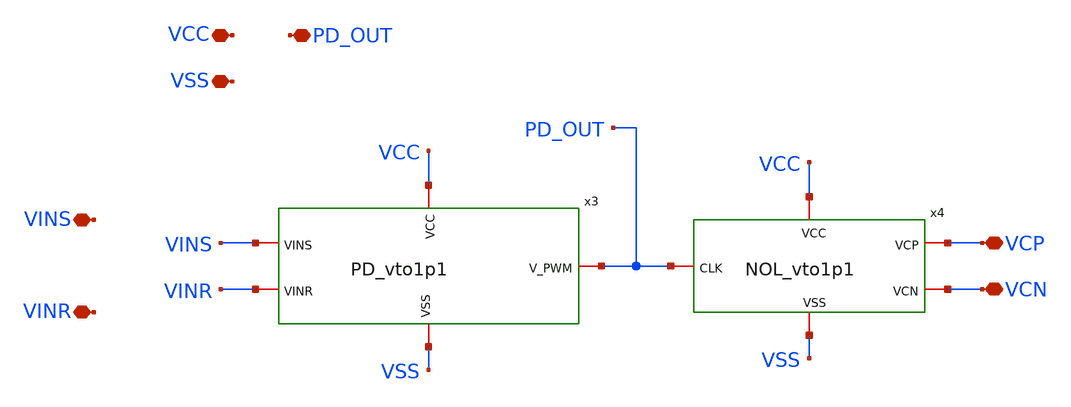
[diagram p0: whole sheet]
** sch_path: AC3E_USM_TDBUCK/design_data/xschem/Digital_Block/DB_sim.sch
* IHP-GmbH/IHP-Open-PDK/ihp-sg13g2/libs.tech/xschem/sg13g2_stdcells/sg13g2_inv_2.sch:
* Copyright 2023 IHP PDK Authors
* Licensed under the Apache License, Version 2.0 (the "License");
**.subckt DB_sim VCC VSS VINS VINR VCP VCN PD_OUT
*.iopin VCC
*.iopin VSS
*.iopin VINS
*.iopin VINR
*.iopin VCP
*.iopin VCN
*.iopin PD_OUT
x3 VCC VSS VINS PD_OUT VINR PD_vto1p1
x4 VCC VSS VCP PD_OUT VCN NOL_vto1p1
**.ends

* expanding   symbol:  ../PD/PD_vto1p1.sym # of pins=5
** sym_path: ../PD/PD_vto1p1.sym
** sch_path: ../PD/PD_vto1p1.sch
.subckt PD_vto1p1 VCC VSS VINS V_PWM VINR
*.iopin V_PWM
*.iopin VCC
*.iopin VSS
*.iopin VINS
*.iopin VINR
C2 VFE1 VSS 100f m=1
C1 VFE1 VSS 100f m=1
x1 V_N net1 VSS VCC VSS VCC V_PWM gf180mcu_fd_sc_mcu9t5v0__nor2_1
x3 VCC VSS VFE1 VINR net2 SPG_vto1p1
x2 VCC VSS VFE1 VINS net1 SPG_vto1p1
x4 net2 V_PWM VSS VCC VSS VCC V_N gf180mcu_fd_sc_mcu9t5v0__nor2_1
.ends


* expanding   symbol:  ../NOL/NOL_vto1p1.sym # of pins=5
** sym_path: AC3E_USM_TDBUCK/design_data/xschem/NOL/NOL_vto1p1.sym
** sch_path: AC3E_USM_TDBUCK/design_data/xschem/NOL/NOL_vto1p1.sch
.subckt NOL_vto1p1 VCC VSS VCP CLK VCN
*.iopin CLK
*.iopin VCP
*.iopin VCN
*.iopin VCC
*.iopin VSS
x5 A1 CLK VCC VSS sg13g2_inv_1
x3 C1 A1 B1 VCC VSS sg13g2_nor2_1
x1 C2 B2 CLK VCC VSS sg13g2_nor2_1
x2 net1 B1 VCC VSS sg13g2_inv_1
x6 net2 B2 VCC VSS sg13g2_inv_2
x7 net3 net1 VCC VSS sg13g2_inv_2
x8 VCN net2 VCC VSS sg13g2_inv_4
x9 VCP net3 VCC VSS sg13g2_inv_4
x10 VCC VSS C1 B2 large_delay_vto1p1
x4 VCC VSS C2 B1 large_delay_vto1p1
.ends


* expanding   symbol:  gf180_digital/SPG/SPG_vto1p1.sym # of pins=5
** sym_path: gf180_digital/SPG/SPG_vto1p1.sym
** sch_path: gf180_digital/SPG/SPG_vto1p1.sch
.subckt SPG_vto1p1 VCC VSS VFE VIN VRE
*.iopin VIN
*.iopin VFE
*.iopin VRE
*.iopin VCC
*.iopin VSS
x1 dly8 dly7 VCC VSS sg13g2_inv_1
x2 net2 predly VCC VSS sg13g2_inv_1
x3 predly net3 VCC VSS sg13g2_inv_1
x4 net1 dly8 VCC VSS sg13g2_inv_1
x5 net3 VIN VCC VSS sg13g2_inv_2
x6 V_gatein predly VCC VSS sg13g2_inv_8
x7 VFE net2 dly8 VCC VSS sg13g2_and2_2
x8 VRE net1 predly VCC VSS sg13g2_and2_2
x9 VCC VSS V_gatein dly7 large_delay_vto1p1
.ends


* expanding   symbol:  sg13g2_stdcells/sg13g2_inv_1.sym # of pins=2
** sym_path: sg13g2_stdcells/sg13g2_inv_1.sym
** sch_path: sg13g2_stdcells/sg13g2_inv_1.sch
.subckt sg13g2_inv_1 Y A VDD VSS
*.opin Y
*.ipin A
*.iopin VDD
*.iopin VSS
XM1 Y A VSS VSS sg13_lv_nmos w=740.00n l=130.00n ng=1 m=1 mm_ok=1
XM2 Y A VDD VDD sg13_lv_pmos w=1.12u l=130.00n ng=1 m=1 mm_ok=1
.ends


* expanding   symbol:  sg13g2_stdcells/sg13g2_nor2_1.sym # of pins=3
** sym_path: sg13g2_stdcells/sg13g2_nor2_1.sym
** sch_path: sg13g2_stdcells/sg13g2_nor2_1.sch
.subckt sg13g2_nor2_1 Y A B VDD VSS
*.opin Y
*.ipin B
*.ipin A
*.iopin VDD
*.iopin VSS
XM1 Y A VSS VSS sg13_lv_nmos w=740.00n l=130.00n ng=1 m=1 mm_ok=1
XM2 Y B VSS VSS sg13_lv_nmos w=740.00n l=130.00n ng=1 m=1 mm_ok=1
XM3 net1 A VDD VDD sg13_lv_pmos w=1.12u l=130.00n ng=1 m=1 mm_ok=1
XM4 Y B net1 VDD sg13_lv_pmos w=1.12u l=130.00n ng=1 m=1 mm_ok=1
.ends


* expanding   symbol:  sg13g2_stdcells/sg13g2_inv_2.sym # of pins=2
** sym_path: sg13g2_stdcells/sg13g2_inv_2.sym
** sch_path: sg13g2_stdcells/sg13g2_inv_2.sch
.subckt sg13g2_inv_2 Y A VDD VSS
*.opin Y
*.ipin A
*.iopin VDD
*.iopin VSS
XM1 Y A VSS VSS sg13_lv_nmos w=1.48u l=130.00n ng=2 m=1 mm_ok=1
XM2 Y A VDD VDD sg13_lv_pmos w=2.24u l=130.00n ng=2 m=1 mm_ok=1
.ends


* expanding   symbol:  sg13g2_stdcells/sg13g2_inv_4.sym # of pins=2
** sym_path: sg13g2_stdcells/sg13g2_inv_4.sym
** sch_path: sg13g2_stdcells/sg13g2_inv_4.sch
.subckt sg13g2_inv_4 Y A VDD VSS
*.ipin A
*.opin Y
*.iopin VDD
*.iopin VSS
XM1 Y A VSS VSS sg13_lv_nmos w=2.96u l=130.00n ng=4 m=1 mm_ok=1
XM2 Y A VDD VDD sg13_lv_pmos w=4.48u l=130.00n ng=4 m=1 mm_ok=1
.ends


* expanding   symbol:  ../large_delay/large_delay_vto1p1.sym # of pins=4
** sym_path: ../large_delay/large_delay_vto1p1.sym
** sch_path: ../large_delay/large_delay_vto1p1.sch
.subckt large_delay_vto1p1 VCC VSS VIN VOUT
*.iopin VIN
*.iopin VOUT
*.iopin VCC
*.iopin VSS
x1[0] n2 VIN VCC VSS sg13g2_dlygate4sd3_1
x1[1] n3 n2 VCC VSS sg13g2_dlygate4sd3_1
x1[2] n4 n3 VCC VSS sg13g2_dlygate4sd3_1
x1[3] n5 n4 VCC VSS sg13g2_dlygate4sd3_1
x1[4] VOUT n5 VCC VSS sg13g2_dlygate4sd3_1
.ends


* expanding   symbol:  sg13g2_stdcells/sg13g2_inv_8.sym # of pins=2
** sym_path: sg13g2_stdcells/sg13g2_inv_8.sym
** sch_path: sg13g2_stdcells/sg13g2_inv_8.sch
.subckt sg13g2_inv_8 Y A VDD VSS
*.opin Y
*.ipin A
*.iopin VDD
*.iopin VSS
XM1 Y A VSS VSS sg13_lv_nmos w=5.92u l=130.00n ng=8 m=1 mm_ok=1
XM2 Y A VDD VDD sg13_lv_pmos w=8.96u l=130.00n ng=8 m=1 mm_ok=1
.ends


* expanding   symbol:  sg13g2_stdcells/sg13g2_and2_2.sym # of pins=3
** sym_path: sg13g2_stdcells/sg13g2_and2_2.sym
** sch_path: sg13g2_stdcells/sg13g2_and2_2.sch
.subckt sg13g2_and2_2 X A B VDD VSS
*.ipin A
*.ipin B
*.opin X
*.iopin VDD
*.iopin VSS
XM1 net1 A net2 VSS sg13_lv_nmos w=640.00n l=130.00n ng=1 m=1 mm_ok=1
XM2 net2 B VSS VSS sg13_lv_nmos w=640.00n l=130.00n ng=1 m=1 mm_ok=1
XM3 X net1 VSS VSS sg13_lv_nmos w=1.48u l=130.00n ng=2 m=1 mm_ok=1
XM4 net1 B VDD VDD sg13_lv_pmos w=840.00n l=130.00n ng=1 m=1 mm_ok=1
XM5 net1 A VDD VDD sg13_lv_pmos w=840.00n l=130.00n ng=1 m=1 mm_ok=1
XM6 X net1 VDD VDD sg13_lv_pmos w=2.24u l=130.00n ng=2 m=1 mm_ok=1
.ends


* expanding   symbol:  sg13g2_stdcells/sg13g2_dlygate4sd3_1.sym # of pins=2
** sym_path: sg13g2_stdcells/sg13g2_dlygate4sd3_1.sym
** sch_path: sg13g2_stdcells/sg13g2_dlygate4sd3_1.sch
.subckt sg13g2_dlygate4sd3_1 X A VDD VSS
*.ipin A
*.opin X
*.iopin VDD
*.iopin VSS
XM1 net3 A VSS VSS sg13_lv_nmos w=420.00n l=130.00n ng=1 m=1 mm_ok=1
XM2 net1 net3 VSS VSS sg13_lv_nmos w=420.00n l=500.0n ng=1 m=1 mm_ok=1
XM3 net2 net1 VSS VSS sg13_lv_nmos w=420.00n l=500.0n ng=1 m=1 mm_ok=1
XM4 X net2 VSS VSS sg13_lv_nmos w=740.00n l=130.00n ng=1 m=1 mm_ok=1
XM5 net3 A VDD VDD sg13_lv_pmos w=420.00n l=130.00n ng=1 m=1 mm_ok=1
XM6 net1 net3 VDD VDD sg13_lv_pmos w=1.000u l=500.0n ng=1 m=1 mm_ok=1
XM7 net2 net1 VDD VDD sg13_lv_pmos w=1.000u l=500.0n ng=1 m=1 mm_ok=1
XM8 X net2 VDD VDD sg13_lv_pmos w=1.12u l=130.00n ng=1 m=1 mm_ok=1
.ends

.end
